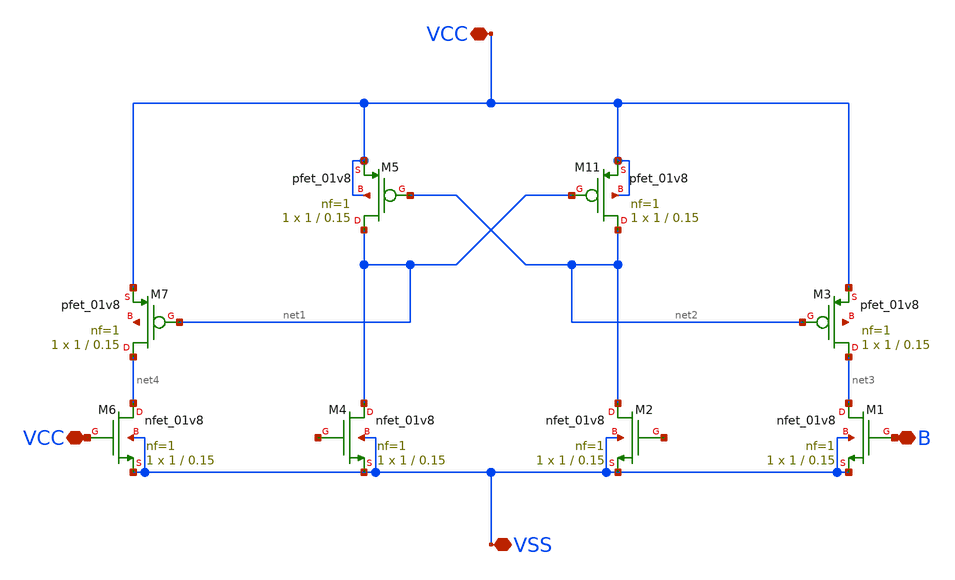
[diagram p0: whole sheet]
** sch_path: RS_latch/RS_latch_old.sch
**.subckt RS_latch_old VCC VSS VCC B
*.iopin VCC
*.iopin VSS
*.iopin VCC
*.iopin B
XM2 net2 net5 VSS VSS sky130_fd_pr__nfet_01v8 L=0.15 W=1 nf=1 ad='int((1 + 1)/2) * 1 / 1 * 0.29' as='int((1 + 2)/2) * 1 / 1 * 0.29'
+ pd='2*int((1 + 1)/2) * (1 / 1 + 0.29)' ps='2*int((1 + 2)/2) * (1 / 1 + 0.29)' nrd='0.29 / 1 ' nrs='0.29 / 1 '
+ sa=0 sb=0 sd=0 mult=1 m=1
XM11 net2 net1 VCC VCC sky130_fd_pr__pfet_01v8 L=0.15 W=1 nf=1 ad='int((nf+1)/2) * W/nf * 0.29' as='int((nf+2)/2) * W/nf * 0.29'
+ pd='2*int((nf+1)/2) * (W/nf + 0.29)' ps='2*int((nf+2)/2) * (W/nf + 0.29)' nrd='0.29 / W' nrs='0.29 / W'
+ sa=0 sb=0 sd=0 mult=1 m=1
XM1 net3 B VSS VSS sky130_fd_pr__nfet_01v8 L=0.15 W=1 nf=1 ad='int((1 + 1)/2) * 1 / 1 * 0.29' as='int((1 + 2)/2) * 1 / 1 * 0.29'
+ pd='2*int((1 + 1)/2) * (1 / 1 + 0.29)' ps='2*int((1 + 2)/2) * (1 / 1 + 0.29)' nrd='0.29 / 1 ' nrs='0.29 / 1 '
+ sa=0 sb=0 sd=0 mult=1 m=1
XM3 net3 net2 VCC net6 sky130_fd_pr__pfet_01v8 L=0.15 W=1 nf=1 ad='int((nf+1)/2) * W/nf * 0.29' as='int((nf+2)/2) * W/nf * 0.29'
+ pd='2*int((nf+1)/2) * (W/nf + 0.29)' ps='2*int((nf+2)/2) * (W/nf + 0.29)' nrd='0.29 / W' nrs='0.29 / W'
+ sa=0 sb=0 sd=0 mult=1 m=1
XM4 net1 net7 VSS VSS sky130_fd_pr__nfet_01v8 L=0.15 W=1 nf=1 ad='int((1 + 1)/2) * 1 / 1 * 0.29' as='int((1 + 2)/2) * 1 / 1 * 0.29'
+ pd='2*int((1 + 1)/2) * (1 / 1 + 0.29)' ps='2*int((1 + 2)/2) * (1 / 1 + 0.29)' nrd='0.29 / 1 ' nrs='0.29 / 1 '
+ sa=0 sb=0 sd=0 mult=1 m=1
XM5 net1 net2 VCC VCC sky130_fd_pr__pfet_01v8 L=0.15 W=1 nf=1 ad='int((nf+1)/2) * W/nf * 0.29' as='int((nf+2)/2) * W/nf * 0.29'
+ pd='2*int((nf+1)/2) * (W/nf + 0.29)' ps='2*int((nf+2)/2) * (W/nf + 0.29)' nrd='0.29 / W' nrs='0.29 / W'
+ sa=0 sb=0 sd=0 mult=1 m=1
XM6 net4 VCC VSS VSS sky130_fd_pr__nfet_01v8 L=0.15 W=1 nf=1 ad='int((1 + 1)/2) * 1 / 1 * 0.29' as='int((1 + 2)/2) * 1 / 1 * 0.29'
+ pd='2*int((1 + 1)/2) * (1 / 1 + 0.29)' ps='2*int((1 + 2)/2) * (1 / 1 + 0.29)' nrd='0.29 / 1 ' nrs='0.29 / 1 '
+ sa=0 sb=0 sd=0 mult=1 m=1
XM7 net4 net1 VCC net8 sky130_fd_pr__pfet_01v8 L=0.15 W=1 nf=1 ad='int((nf+1)/2) * W/nf * 0.29' as='int((nf+2)/2) * W/nf * 0.29'
+ pd='2*int((nf+1)/2) * (W/nf + 0.29)' ps='2*int((nf+2)/2) * (W/nf + 0.29)' nrd='0.29 / W' nrs='0.29 / W'
+ sa=0 sb=0 sd=0 mult=1 m=1
**.ends
.end
